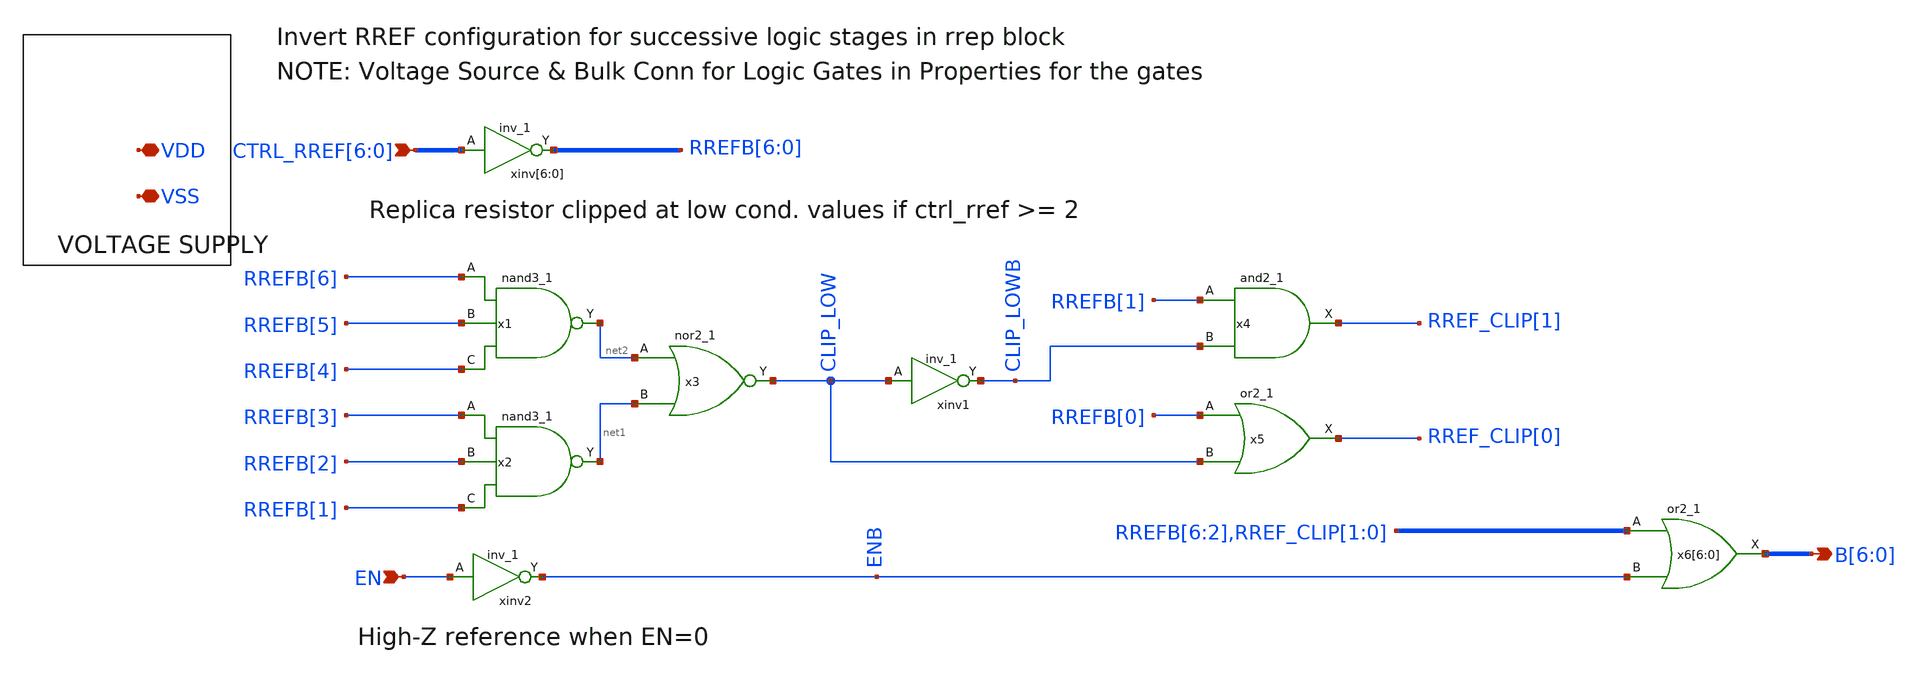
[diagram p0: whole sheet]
** sch_path: BL_Read_Interface/rram_read_csa_rrep_digital.sch
**.subckt rram_read_csa_rrep_digital VSS VDD
*+ CTRL_RREF[6],CTRL_RREF[5],CTRL_RREF[4],CTRL_RREF[3],CTRL_RREF[2],CTRL_RREF[1],CTRL_RREF[0] EN B[6],B[5],B[4],B[3],B[2],B[1],B[0]
*.iopin VSS
*.iopin VDD
*.ipin CTRL_RREF[6],CTRL_RREF[5],CTRL_RREF[4],CTRL_RREF[3],CTRL_RREF[2],CTRL_RREF[1],CTRL_RREF[0]
*.ipin EN
*.opin B[6],B[5],B[4],B[3],B[2],B[1],B[0]
xinv[6] CTRL_RREF[6] VSS VSS VDD VDD RREFB[6] sky130_fd_sc_hd__inv_1
xinv[5] CTRL_RREF[5] VSS VSS VDD VDD RREFB[5] sky130_fd_sc_hd__inv_1
xinv[4] CTRL_RREF[4] VSS VSS VDD VDD RREFB[4] sky130_fd_sc_hd__inv_1
xinv[3] CTRL_RREF[3] VSS VSS VDD VDD RREFB[3] sky130_fd_sc_hd__inv_1
xinv[2] CTRL_RREF[2] VSS VSS VDD VDD RREFB[2] sky130_fd_sc_hd__inv_1
xinv[1] CTRL_RREF[1] VSS VSS VDD VDD RREFB[1] sky130_fd_sc_hd__inv_1
xinv[0] CTRL_RREF[0] VSS VSS VDD VDD RREFB[0] sky130_fd_sc_hd__inv_1
x1 RREFB[6] RREFB[5] RREFB[4] VSS VSS VDD VDD net2 sky130_fd_sc_hd__nand3_1
x2 RREFB[3] RREFB[2] RREFB[1] VSS VSS VDD VDD net1 sky130_fd_sc_hd__nand3_1
x3 net2 net1 VSS VSS VDD VDD CLIP_LOW sky130_fd_sc_hd__nor2_1
xinv1 CLIP_LOW VSS VSS VDD VDD CLIP_LOWB sky130_fd_sc_hd__inv_1
xinv2 EN VSS VSS VDD VDD ENB sky130_fd_sc_hd__inv_1
x4 RREFB[1] CLIP_LOWB VSS VSS VDD VDD RREF_CLIP[1] sky130_fd_sc_hd__and2_1
x5 RREFB[0] CLIP_LOW VSS VSS VDD VDD RREF_CLIP[0] sky130_fd_sc_hd__or2_1
x6[6] RREFB[6] ENB VSS VSS VDD VDD B[6] sky130_fd_sc_hd__or2_1
x6[5] RREFB[5] ENB VSS VSS VDD VDD B[5] sky130_fd_sc_hd__or2_1
x6[4] RREFB[4] ENB VSS VSS VDD VDD B[4] sky130_fd_sc_hd__or2_1
x6[3] RREFB[3] ENB VSS VSS VDD VDD B[3] sky130_fd_sc_hd__or2_1
x6[2] RREFB[2] ENB VSS VSS VDD VDD B[2] sky130_fd_sc_hd__or2_1
x6[1] RREF_CLIP[1] ENB VSS VSS VDD VDD B[1] sky130_fd_sc_hd__or2_1
x6[0] RREF_CLIP[0] ENB VSS VSS VDD VDD B[0] sky130_fd_sc_hd__or2_1
**.ends
.end
